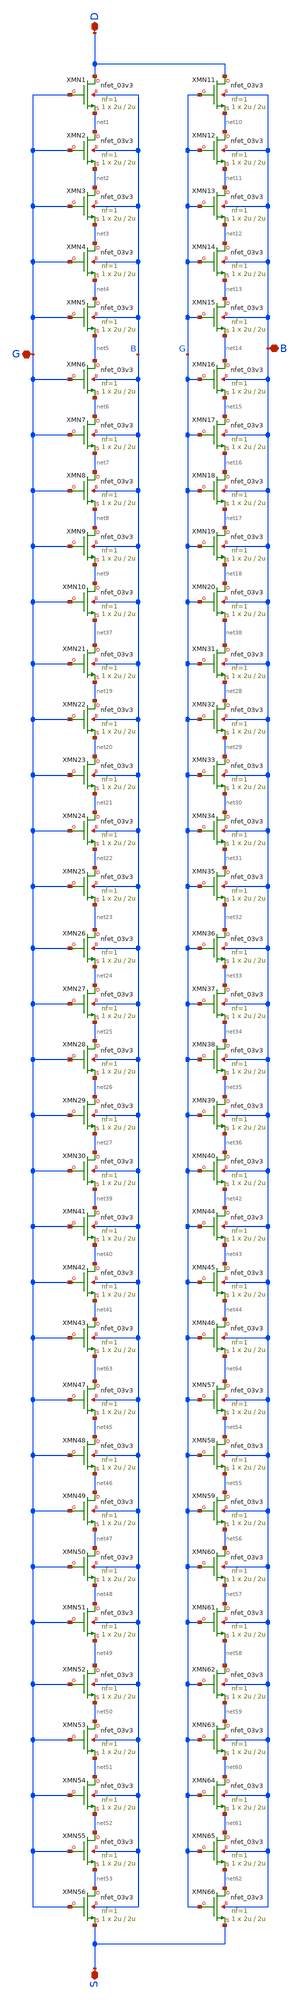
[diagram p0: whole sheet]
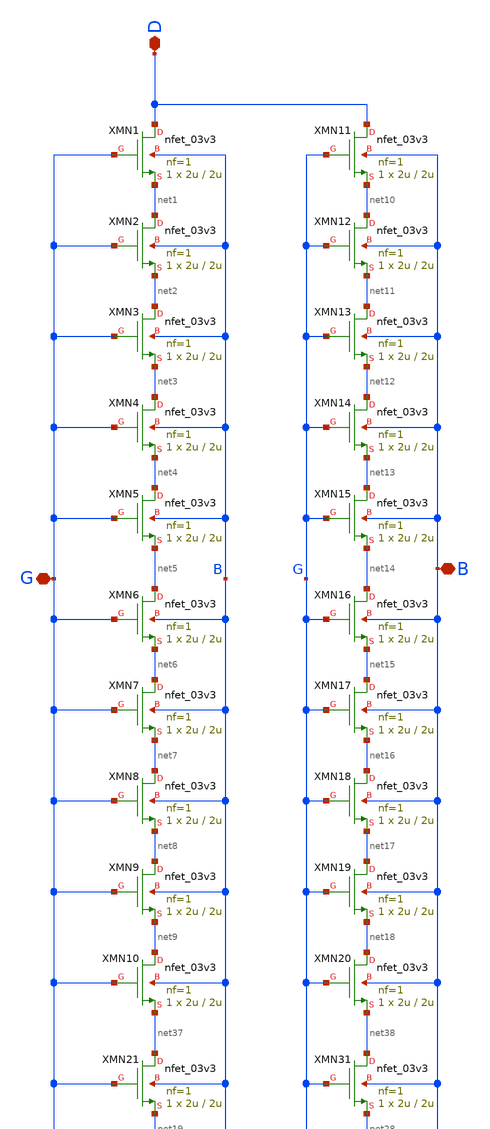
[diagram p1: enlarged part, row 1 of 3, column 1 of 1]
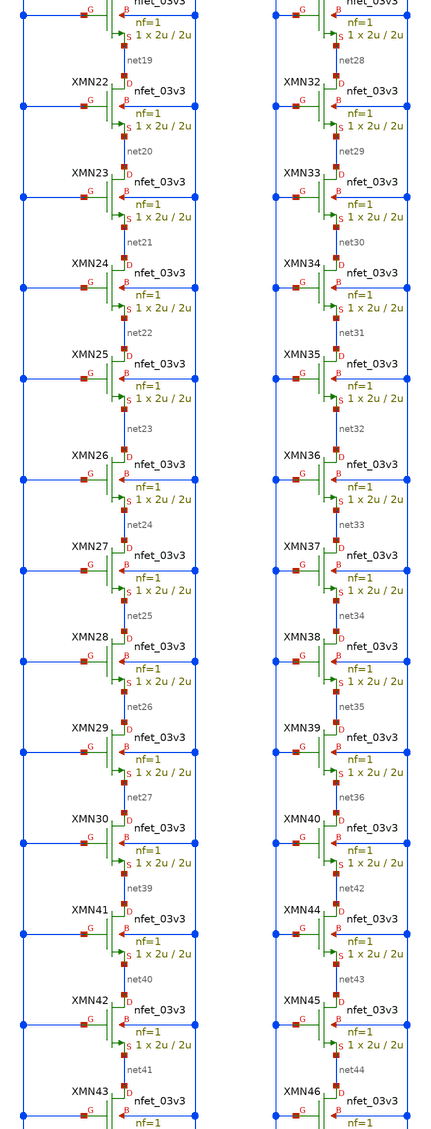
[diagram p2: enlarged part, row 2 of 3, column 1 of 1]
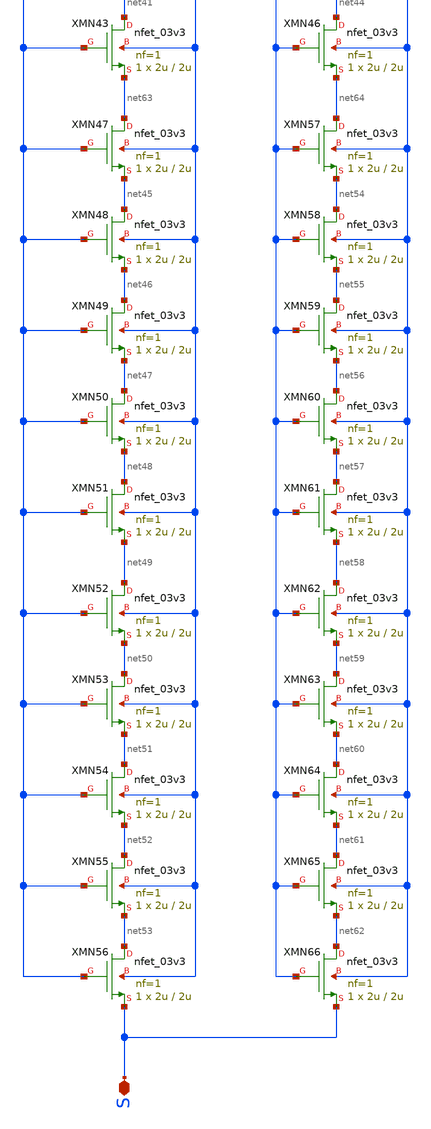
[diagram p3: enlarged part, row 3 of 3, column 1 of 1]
** sch_path: Voltage_Reference/symbols_vr/NMOS_matrix1_SCM1.sch
**.subckt NMOS_matrix1_SCM1 D G S B
*.iopin D
*.iopin G
*.iopin S
*.iopin B
XMN1 D G net1 B nfet_03v3 L=2u W=2u nf=1 ad='int((nf+1)/2) * W/nf * 0.18u' as='int((nf+2)/2) * W/nf * 0.18u'
+ pd='2*int((nf+1)/2) * (W/nf + 0.18u)' ps='2*int((nf+2)/2) * (W/nf + 0.18u)' nrd='0.18u / W' nrs='0.18u / W'
+ sa=0 sb=0 sd=0 m=1
XMN2 net1 G net2 B nfet_03v3 L=2u W=2u nf=1 ad='int((nf+1)/2) * W/nf * 0.18u' as='int((nf+2)/2) * W/nf * 0.18u'
+ pd='2*int((nf+1)/2) * (W/nf + 0.18u)' ps='2*int((nf+2)/2) * (W/nf + 0.18u)' nrd='0.18u / W' nrs='0.18u / W'
+ sa=0 sb=0 sd=0 m=1
XMN3 net2 G net3 B nfet_03v3 L=2u W=2u nf=1 ad='int((nf+1)/2) * W/nf * 0.18u' as='int((nf+2)/2) * W/nf * 0.18u'
+ pd='2*int((nf+1)/2) * (W/nf + 0.18u)' ps='2*int((nf+2)/2) * (W/nf + 0.18u)' nrd='0.18u / W' nrs='0.18u / W'
+ sa=0 sb=0 sd=0 m=1
XMN4 net3 G net4 B nfet_03v3 L=2u W=2u nf=1 ad='int((nf+1)/2) * W/nf * 0.18u' as='int((nf+2)/2) * W/nf * 0.18u'
+ pd='2*int((nf+1)/2) * (W/nf + 0.18u)' ps='2*int((nf+2)/2) * (W/nf + 0.18u)' nrd='0.18u / W' nrs='0.18u / W'
+ sa=0 sb=0 sd=0 m=1
XMN5 net4 G net5 B nfet_03v3 L=2u W=2u nf=1 ad='int((nf+1)/2) * W/nf * 0.18u' as='int((nf+2)/2) * W/nf * 0.18u'
+ pd='2*int((nf+1)/2) * (W/nf + 0.18u)' ps='2*int((nf+2)/2) * (W/nf + 0.18u)' nrd='0.18u / W' nrs='0.18u / W'
+ sa=0 sb=0 sd=0 m=1
XMN6 net5 G net6 B nfet_03v3 L=2u W=2u nf=1 ad='int((nf+1)/2) * W/nf * 0.18u' as='int((nf+2)/2) * W/nf * 0.18u'
+ pd='2*int((nf+1)/2) * (W/nf + 0.18u)' ps='2*int((nf+2)/2) * (W/nf + 0.18u)' nrd='0.18u / W' nrs='0.18u / W'
+ sa=0 sb=0 sd=0 m=1
XMN7 net6 G net7 B nfet_03v3 L=2u W=2u nf=1 ad='int((nf+1)/2) * W/nf * 0.18u' as='int((nf+2)/2) * W/nf * 0.18u'
+ pd='2*int((nf+1)/2) * (W/nf + 0.18u)' ps='2*int((nf+2)/2) * (W/nf + 0.18u)' nrd='0.18u / W' nrs='0.18u / W'
+ sa=0 sb=0 sd=0 m=1
XMN8 net7 G net8 B nfet_03v3 L=2u W=2u nf=1 ad='int((nf+1)/2) * W/nf * 0.18u' as='int((nf+2)/2) * W/nf * 0.18u'
+ pd='2*int((nf+1)/2) * (W/nf + 0.18u)' ps='2*int((nf+2)/2) * (W/nf + 0.18u)' nrd='0.18u / W' nrs='0.18u / W'
+ sa=0 sb=0 sd=0 m=1
XMN9 net8 G net9 B nfet_03v3 L=2u W=2u nf=1 ad='int((nf+1)/2) * W/nf * 0.18u' as='int((nf+2)/2) * W/nf * 0.18u'
+ pd='2*int((nf+1)/2) * (W/nf + 0.18u)' ps='2*int((nf+2)/2) * (W/nf + 0.18u)' nrd='0.18u / W' nrs='0.18u / W'
+ sa=0 sb=0 sd=0 m=1
XMN10 net9 G net37 B nfet_03v3 L=2u W=2u nf=1 ad='int((nf+1)/2) * W/nf * 0.18u' as='int((nf+2)/2) * W/nf * 0.18u'
+ pd='2*int((nf+1)/2) * (W/nf + 0.18u)' ps='2*int((nf+2)/2) * (W/nf + 0.18u)' nrd='0.18u / W' nrs='0.18u / W'
+ sa=0 sb=0 sd=0 m=1
XMN11 D G net10 B nfet_03v3 L=2u W=2u nf=1 ad='int((nf+1)/2) * W/nf * 0.18u' as='int((nf+2)/2) * W/nf * 0.18u'
+ pd='2*int((nf+1)/2) * (W/nf + 0.18u)' ps='2*int((nf+2)/2) * (W/nf + 0.18u)' nrd='0.18u / W' nrs='0.18u / W'
+ sa=0 sb=0 sd=0 m=1
XMN12 net10 G net11 B nfet_03v3 L=2u W=2u nf=1 ad='int((nf+1)/2) * W/nf * 0.18u' as='int((nf+2)/2) * W/nf * 0.18u'
+ pd='2*int((nf+1)/2) * (W/nf + 0.18u)' ps='2*int((nf+2)/2) * (W/nf + 0.18u)' nrd='0.18u / W' nrs='0.18u / W'
+ sa=0 sb=0 sd=0 m=1
XMN13 net11 G net12 B nfet_03v3 L=2u W=2u nf=1 ad='int((nf+1)/2) * W/nf * 0.18u' as='int((nf+2)/2) * W/nf * 0.18u'
+ pd='2*int((nf+1)/2) * (W/nf + 0.18u)' ps='2*int((nf+2)/2) * (W/nf + 0.18u)' nrd='0.18u / W' nrs='0.18u / W'
+ sa=0 sb=0 sd=0 m=1
XMN14 net12 G net13 B nfet_03v3 L=2u W=2u nf=1 ad='int((nf+1)/2) * W/nf * 0.18u' as='int((nf+2)/2) * W/nf * 0.18u'
+ pd='2*int((nf+1)/2) * (W/nf + 0.18u)' ps='2*int((nf+2)/2) * (W/nf + 0.18u)' nrd='0.18u / W' nrs='0.18u / W'
+ sa=0 sb=0 sd=0 m=1
XMN15 net13 G net14 B nfet_03v3 L=2u W=2u nf=1 ad='int((nf+1)/2) * W/nf * 0.18u' as='int((nf+2)/2) * W/nf * 0.18u'
+ pd='2*int((nf+1)/2) * (W/nf + 0.18u)' ps='2*int((nf+2)/2) * (W/nf + 0.18u)' nrd='0.18u / W' nrs='0.18u / W'
+ sa=0 sb=0 sd=0 m=1
XMN16 net14 G net15 B nfet_03v3 L=2u W=2u nf=1 ad='int((nf+1)/2) * W/nf * 0.18u' as='int((nf+2)/2) * W/nf * 0.18u'
+ pd='2*int((nf+1)/2) * (W/nf + 0.18u)' ps='2*int((nf+2)/2) * (W/nf + 0.18u)' nrd='0.18u / W' nrs='0.18u / W'
+ sa=0 sb=0 sd=0 m=1
XMN17 net15 G net16 B nfet_03v3 L=2u W=2u nf=1 ad='int((nf+1)/2) * W/nf * 0.18u' as='int((nf+2)/2) * W/nf * 0.18u'
+ pd='2*int((nf+1)/2) * (W/nf + 0.18u)' ps='2*int((nf+2)/2) * (W/nf + 0.18u)' nrd='0.18u / W' nrs='0.18u / W'
+ sa=0 sb=0 sd=0 m=1
XMN18 net16 G net17 B nfet_03v3 L=2u W=2u nf=1 ad='int((nf+1)/2) * W/nf * 0.18u' as='int((nf+2)/2) * W/nf * 0.18u'
+ pd='2*int((nf+1)/2) * (W/nf + 0.18u)' ps='2*int((nf+2)/2) * (W/nf + 0.18u)' nrd='0.18u / W' nrs='0.18u / W'
+ sa=0 sb=0 sd=0 m=1
XMN19 net17 G net18 B nfet_03v3 L=2u W=2u nf=1 ad='int((nf+1)/2) * W/nf * 0.18u' as='int((nf+2)/2) * W/nf * 0.18u'
+ pd='2*int((nf+1)/2) * (W/nf + 0.18u)' ps='2*int((nf+2)/2) * (W/nf + 0.18u)' nrd='0.18u / W' nrs='0.18u / W'
+ sa=0 sb=0 sd=0 m=1
XMN20 net18 G net38 B nfet_03v3 L=2u W=2u nf=1 ad='int((nf+1)/2) * W/nf * 0.18u' as='int((nf+2)/2) * W/nf * 0.18u'
+ pd='2*int((nf+1)/2) * (W/nf + 0.18u)' ps='2*int((nf+2)/2) * (W/nf + 0.18u)' nrd='0.18u / W' nrs='0.18u / W'
+ sa=0 sb=0 sd=0 m=1
XMN21 net37 G net19 B nfet_03v3 L=2u W=2u nf=1 ad='int((nf+1)/2) * W/nf * 0.18u' as='int((nf+2)/2) * W/nf * 0.18u'
+ pd='2*int((nf+1)/2) * (W/nf + 0.18u)' ps='2*int((nf+2)/2) * (W/nf + 0.18u)' nrd='0.18u / W' nrs='0.18u / W'
+ sa=0 sb=0 sd=0 m=1
XMN22 net19 G net20 B nfet_03v3 L=2u W=2u nf=1 ad='int((nf+1)/2) * W/nf * 0.18u' as='int((nf+2)/2) * W/nf * 0.18u'
+ pd='2*int((nf+1)/2) * (W/nf + 0.18u)' ps='2*int((nf+2)/2) * (W/nf + 0.18u)' nrd='0.18u / W' nrs='0.18u / W'
+ sa=0 sb=0 sd=0 m=1
XMN23 net20 G net21 B nfet_03v3 L=2u W=2u nf=1 ad='int((nf+1)/2) * W/nf * 0.18u' as='int((nf+2)/2) * W/nf * 0.18u'
+ pd='2*int((nf+1)/2) * (W/nf + 0.18u)' ps='2*int((nf+2)/2) * (W/nf + 0.18u)' nrd='0.18u / W' nrs='0.18u / W'
+ sa=0 sb=0 sd=0 m=1
XMN24 net21 G net22 B nfet_03v3 L=2u W=2u nf=1 ad='int((nf+1)/2) * W/nf * 0.18u' as='int((nf+2)/2) * W/nf * 0.18u'
+ pd='2*int((nf+1)/2) * (W/nf + 0.18u)' ps='2*int((nf+2)/2) * (W/nf + 0.18u)' nrd='0.18u / W' nrs='0.18u / W'
+ sa=0 sb=0 sd=0 m=1
XMN25 net22 G net23 B nfet_03v3 L=2u W=2u nf=1 ad='int((nf+1)/2) * W/nf * 0.18u' as='int((nf+2)/2) * W/nf * 0.18u'
+ pd='2*int((nf+1)/2) * (W/nf + 0.18u)' ps='2*int((nf+2)/2) * (W/nf + 0.18u)' nrd='0.18u / W' nrs='0.18u / W'
+ sa=0 sb=0 sd=0 m=1
XMN26 net23 G net24 B nfet_03v3 L=2u W=2u nf=1 ad='int((nf+1)/2) * W/nf * 0.18u' as='int((nf+2)/2) * W/nf * 0.18u'
+ pd='2*int((nf+1)/2) * (W/nf + 0.18u)' ps='2*int((nf+2)/2) * (W/nf + 0.18u)' nrd='0.18u / W' nrs='0.18u / W'
+ sa=0 sb=0 sd=0 m=1
XMN27 net24 G net25 B nfet_03v3 L=2u W=2u nf=1 ad='int((nf+1)/2) * W/nf * 0.18u' as='int((nf+2)/2) * W/nf * 0.18u'
+ pd='2*int((nf+1)/2) * (W/nf + 0.18u)' ps='2*int((nf+2)/2) * (W/nf + 0.18u)' nrd='0.18u / W' nrs='0.18u / W'
+ sa=0 sb=0 sd=0 m=1
XMN28 net25 G net26 B nfet_03v3 L=2u W=2u nf=1 ad='int((nf+1)/2) * W/nf * 0.18u' as='int((nf+2)/2) * W/nf * 0.18u'
+ pd='2*int((nf+1)/2) * (W/nf + 0.18u)' ps='2*int((nf+2)/2) * (W/nf + 0.18u)' nrd='0.18u / W' nrs='0.18u / W'
+ sa=0 sb=0 sd=0 m=1
XMN29 net26 G net27 B nfet_03v3 L=2u W=2u nf=1 ad='int((nf+1)/2) * W/nf * 0.18u' as='int((nf+2)/2) * W/nf * 0.18u'
+ pd='2*int((nf+1)/2) * (W/nf + 0.18u)' ps='2*int((nf+2)/2) * (W/nf + 0.18u)' nrd='0.18u / W' nrs='0.18u / W'
+ sa=0 sb=0 sd=0 m=1
XMN30 net27 G net39 B nfet_03v3 L=2u W=2u nf=1 ad='int((nf+1)/2) * W/nf * 0.18u' as='int((nf+2)/2) * W/nf * 0.18u'
+ pd='2*int((nf+1)/2) * (W/nf + 0.18u)' ps='2*int((nf+2)/2) * (W/nf + 0.18u)' nrd='0.18u / W' nrs='0.18u / W'
+ sa=0 sb=0 sd=0 m=1
XMN31 net38 G net28 B nfet_03v3 L=2u W=2u nf=1 ad='int((nf+1)/2) * W/nf * 0.18u' as='int((nf+2)/2) * W/nf * 0.18u'
+ pd='2*int((nf+1)/2) * (W/nf + 0.18u)' ps='2*int((nf+2)/2) * (W/nf + 0.18u)' nrd='0.18u / W' nrs='0.18u / W'
+ sa=0 sb=0 sd=0 m=1
XMN32 net28 G net29 B nfet_03v3 L=2u W=2u nf=1 ad='int((nf+1)/2) * W/nf * 0.18u' as='int((nf+2)/2) * W/nf * 0.18u'
+ pd='2*int((nf+1)/2) * (W/nf + 0.18u)' ps='2*int((nf+2)/2) * (W/nf + 0.18u)' nrd='0.18u / W' nrs='0.18u / W'
+ sa=0 sb=0 sd=0 m=1
XMN33 net29 G net30 B nfet_03v3 L=2u W=2u nf=1 ad='int((nf+1)/2) * W/nf * 0.18u' as='int((nf+2)/2) * W/nf * 0.18u'
+ pd='2*int((nf+1)/2) * (W/nf + 0.18u)' ps='2*int((nf+2)/2) * (W/nf + 0.18u)' nrd='0.18u / W' nrs='0.18u / W'
+ sa=0 sb=0 sd=0 m=1
XMN34 net30 G net31 B nfet_03v3 L=2u W=2u nf=1 ad='int((nf+1)/2) * W/nf * 0.18u' as='int((nf+2)/2) * W/nf * 0.18u'
+ pd='2*int((nf+1)/2) * (W/nf + 0.18u)' ps='2*int((nf+2)/2) * (W/nf + 0.18u)' nrd='0.18u / W' nrs='0.18u / W'
+ sa=0 sb=0 sd=0 m=1
XMN35 net31 G net32 B nfet_03v3 L=2u W=2u nf=1 ad='int((nf+1)/2) * W/nf * 0.18u' as='int((nf+2)/2) * W/nf * 0.18u'
+ pd='2*int((nf+1)/2) * (W/nf + 0.18u)' ps='2*int((nf+2)/2) * (W/nf + 0.18u)' nrd='0.18u / W' nrs='0.18u / W'
+ sa=0 sb=0 sd=0 m=1
XMN36 net32 G net33 B nfet_03v3 L=2u W=2u nf=1 ad='int((nf+1)/2) * W/nf * 0.18u' as='int((nf+2)/2) * W/nf * 0.18u'
+ pd='2*int((nf+1)/2) * (W/nf + 0.18u)' ps='2*int((nf+2)/2) * (W/nf + 0.18u)' nrd='0.18u / W' nrs='0.18u / W'
+ sa=0 sb=0 sd=0 m=1
XMN37 net33 G net34 B nfet_03v3 L=2u W=2u nf=1 ad='int((nf+1)/2) * W/nf * 0.18u' as='int((nf+2)/2) * W/nf * 0.18u'
+ pd='2*int((nf+1)/2) * (W/nf + 0.18u)' ps='2*int((nf+2)/2) * (W/nf + 0.18u)' nrd='0.18u / W' nrs='0.18u / W'
+ sa=0 sb=0 sd=0 m=1
XMN38 net34 G net35 B nfet_03v3 L=2u W=2u nf=1 ad='int((nf+1)/2) * W/nf * 0.18u' as='int((nf+2)/2) * W/nf * 0.18u'
+ pd='2*int((nf+1)/2) * (W/nf + 0.18u)' ps='2*int((nf+2)/2) * (W/nf + 0.18u)' nrd='0.18u / W' nrs='0.18u / W'
+ sa=0 sb=0 sd=0 m=1
XMN39 net35 G net36 B nfet_03v3 L=2u W=2u nf=1 ad='int((nf+1)/2) * W/nf * 0.18u' as='int((nf+2)/2) * W/nf * 0.18u'
+ pd='2*int((nf+1)/2) * (W/nf + 0.18u)' ps='2*int((nf+2)/2) * (W/nf + 0.18u)' nrd='0.18u / W' nrs='0.18u / W'
+ sa=0 sb=0 sd=0 m=1
XMN40 net36 G net42 B nfet_03v3 L=2u W=2u nf=1 ad='int((nf+1)/2) * W/nf * 0.18u' as='int((nf+2)/2) * W/nf * 0.18u'
+ pd='2*int((nf+1)/2) * (W/nf + 0.18u)' ps='2*int((nf+2)/2) * (W/nf + 0.18u)' nrd='0.18u / W' nrs='0.18u / W'
+ sa=0 sb=0 sd=0 m=1
XMN41 net39 G net40 B nfet_03v3 L=2u W=2u nf=1 ad='int((nf+1)/2) * W/nf * 0.18u' as='int((nf+2)/2) * W/nf * 0.18u'
+ pd='2*int((nf+1)/2) * (W/nf + 0.18u)' ps='2*int((nf+2)/2) * (W/nf + 0.18u)' nrd='0.18u / W' nrs='0.18u / W'
+ sa=0 sb=0 sd=0 m=1
XMN42 net40 G net41 B nfet_03v3 L=2u W=2u nf=1 ad='int((nf+1)/2) * W/nf * 0.18u' as='int((nf+2)/2) * W/nf * 0.18u'
+ pd='2*int((nf+1)/2) * (W/nf + 0.18u)' ps='2*int((nf+2)/2) * (W/nf + 0.18u)' nrd='0.18u / W' nrs='0.18u / W'
+ sa=0 sb=0 sd=0 m=1
XMN43 net41 G net63 B nfet_03v3 L=2u W=2u nf=1 ad='int((nf+1)/2) * W/nf * 0.18u' as='int((nf+2)/2) * W/nf * 0.18u'
+ pd='2*int((nf+1)/2) * (W/nf + 0.18u)' ps='2*int((nf+2)/2) * (W/nf + 0.18u)' nrd='0.18u / W' nrs='0.18u / W'
+ sa=0 sb=0 sd=0 m=1
XMN44 net42 G net43 B nfet_03v3 L=2u W=2u nf=1 ad='int((nf+1)/2) * W/nf * 0.18u' as='int((nf+2)/2) * W/nf * 0.18u'
+ pd='2*int((nf+1)/2) * (W/nf + 0.18u)' ps='2*int((nf+2)/2) * (W/nf + 0.18u)' nrd='0.18u / W' nrs='0.18u / W'
+ sa=0 sb=0 sd=0 m=1
XMN45 net43 G net44 B nfet_03v3 L=2u W=2u nf=1 ad='int((nf+1)/2) * W/nf * 0.18u' as='int((nf+2)/2) * W/nf * 0.18u'
+ pd='2*int((nf+1)/2) * (W/nf + 0.18u)' ps='2*int((nf+2)/2) * (W/nf + 0.18u)' nrd='0.18u / W' nrs='0.18u / W'
+ sa=0 sb=0 sd=0 m=1
XMN46 net44 G net64 B nfet_03v3 L=2u W=2u nf=1 ad='int((nf+1)/2) * W/nf * 0.18u' as='int((nf+2)/2) * W/nf * 0.18u'
+ pd='2*int((nf+1)/2) * (W/nf + 0.18u)' ps='2*int((nf+2)/2) * (W/nf + 0.18u)' nrd='0.18u / W' nrs='0.18u / W'
+ sa=0 sb=0 sd=0 m=1
XMN47 net63 G net45 B nfet_03v3 L=2u W=2u nf=1 ad='int((nf+1)/2) * W/nf * 0.18u' as='int((nf+2)/2) * W/nf * 0.18u'
+ pd='2*int((nf+1)/2) * (W/nf + 0.18u)' ps='2*int((nf+2)/2) * (W/nf + 0.18u)' nrd='0.18u / W' nrs='0.18u / W'
+ sa=0 sb=0 sd=0 m=1
XMN48 net45 G net46 B nfet_03v3 L=2u W=2u nf=1 ad='int((nf+1)/2) * W/nf * 0.18u' as='int((nf+2)/2) * W/nf * 0.18u'
+ pd='2*int((nf+1)/2) * (W/nf + 0.18u)' ps='2*int((nf+2)/2) * (W/nf + 0.18u)' nrd='0.18u / W' nrs='0.18u / W'
+ sa=0 sb=0 sd=0 m=1
XMN49 net46 G net47 B nfet_03v3 L=2u W=2u nf=1 ad='int((nf+1)/2) * W/nf * 0.18u' as='int((nf+2)/2) * W/nf * 0.18u'
+ pd='2*int((nf+1)/2) * (W/nf + 0.18u)' ps='2*int((nf+2)/2) * (W/nf + 0.18u)' nrd='0.18u / W' nrs='0.18u / W'
+ sa=0 sb=0 sd=0 m=1
XMN50 net47 G net48 B nfet_03v3 L=2u W=2u nf=1 ad='int((nf+1)/2) * W/nf * 0.18u' as='int((nf+2)/2) * W/nf * 0.18u'
+ pd='2*int((nf+1)/2) * (W/nf + 0.18u)' ps='2*int((nf+2)/2) * (W/nf + 0.18u)' nrd='0.18u / W' nrs='0.18u / W'
+ sa=0 sb=0 sd=0 m=1
XMN51 net48 G net49 B nfet_03v3 L=2u W=2u nf=1 ad='int((nf+1)/2) * W/nf * 0.18u' as='int((nf+2)/2) * W/nf * 0.18u'
+ pd='2*int((nf+1)/2) * (W/nf + 0.18u)' ps='2*int((nf+2)/2) * (W/nf + 0.18u)' nrd='0.18u / W' nrs='0.18u / W'
+ sa=0 sb=0 sd=0 m=1
XMN52 net49 G net50 B nfet_03v3 L=2u W=2u nf=1 ad='int((nf+1)/2) * W/nf * 0.18u' as='int((nf+2)/2) * W/nf * 0.18u'
+ pd='2*int((nf+1)/2) * (W/nf + 0.18u)' ps='2*int((nf+2)/2) * (W/nf + 0.18u)' nrd='0.18u / W' nrs='0.18u / W'
+ sa=0 sb=0 sd=0 m=1
XMN53 net50 G net51 B nfet_03v3 L=2u W=2u nf=1 ad='int((nf+1)/2) * W/nf * 0.18u' as='int((nf+2)/2) * W/nf * 0.18u'
+ pd='2*int((nf+1)/2) * (W/nf + 0.18u)' ps='2*int((nf+2)/2) * (W/nf + 0.18u)' nrd='0.18u / W' nrs='0.18u / W'
+ sa=0 sb=0 sd=0 m=1
XMN54 net51 G net52 B nfet_03v3 L=2u W=2u nf=1 ad='int((nf+1)/2) * W/nf * 0.18u' as='int((nf+2)/2) * W/nf * 0.18u'
+ pd='2*int((nf+1)/2) * (W/nf + 0.18u)' ps='2*int((nf+2)/2) * (W/nf + 0.18u)' nrd='0.18u / W' nrs='0.18u / W'
+ sa=0 sb=0 sd=0 m=1
XMN55 net52 G net53 B nfet_03v3 L=2u W=2u nf=1 ad='int((nf+1)/2) * W/nf * 0.18u' as='int((nf+2)/2) * W/nf * 0.18u'
+ pd='2*int((nf+1)/2) * (W/nf + 0.18u)' ps='2*int((nf+2)/2) * (W/nf + 0.18u)' nrd='0.18u / W' nrs='0.18u / W'
+ sa=0 sb=0 sd=0 m=1
XMN56 net53 G S B nfet_03v3 L=2u W=2u nf=1 ad='int((nf+1)/2) * W/nf * 0.18u' as='int((nf+2)/2) * W/nf * 0.18u'
+ pd='2*int((nf+1)/2) * (W/nf + 0.18u)' ps='2*int((nf+2)/2) * (W/nf + 0.18u)' nrd='0.18u / W' nrs='0.18u / W'
+ sa=0 sb=0 sd=0 m=1
XMN57 net64 G net54 B nfet_03v3 L=2u W=2u nf=1 ad='int((nf+1)/2) * W/nf * 0.18u' as='int((nf+2)/2) * W/nf * 0.18u'
+ pd='2*int((nf+1)/2) * (W/nf + 0.18u)' ps='2*int((nf+2)/2) * (W/nf + 0.18u)' nrd='0.18u / W' nrs='0.18u / W'
+ sa=0 sb=0 sd=0 m=1
XMN58 net54 G net55 B nfet_03v3 L=2u W=2u nf=1 ad='int((nf+1)/2) * W/nf * 0.18u' as='int((nf+2)/2) * W/nf * 0.18u'
+ pd='2*int((nf+1)/2) * (W/nf + 0.18u)' ps='2*int((nf+2)/2) * (W/nf + 0.18u)' nrd='0.18u / W' nrs='0.18u / W'
+ sa=0 sb=0 sd=0 m=1
XMN59 net55 G net56 B nfet_03v3 L=2u W=2u nf=1 ad='int((nf+1)/2) * W/nf * 0.18u' as='int((nf+2)/2) * W/nf * 0.18u'
+ pd='2*int((nf+1)/2) * (W/nf + 0.18u)' ps='2*int((nf+2)/2) * (W/nf + 0.18u)' nrd='0.18u / W' nrs='0.18u / W'
+ sa=0 sb=0 sd=0 m=1
XMN60 net56 G net57 B nfet_03v3 L=2u W=2u nf=1 ad='int((nf+1)/2) * W/nf * 0.18u' as='int((nf+2)/2) * W/nf * 0.18u'
+ pd='2*int((nf+1)/2) * (W/nf + 0.18u)' ps='2*int((nf+2)/2) * (W/nf + 0.18u)' nrd='0.18u / W' nrs='0.18u / W'
+ sa=0 sb=0 sd=0 m=1
XMN61 net57 G net58 B nfet_03v3 L=2u W=2u nf=1 ad='int((nf+1)/2) * W/nf * 0.18u' as='int((nf+2)/2) * W/nf * 0.18u'
+ pd='2*int((nf+1)/2) * (W/nf + 0.18u)' ps='2*int((nf+2)/2) * (W/nf + 0.18u)' nrd='0.18u / W' nrs='0.18u / W'
+ sa=0 sb=0 sd=0 m=1
XMN62 net58 G net59 B nfet_03v3 L=2u W=2u nf=1 ad='int((nf+1)/2) * W/nf * 0.18u' as='int((nf+2)/2) * W/nf * 0.18u'
+ pd='2*int((nf+1)/2) * (W/nf + 0.18u)' ps='2*int((nf+2)/2) * (W/nf + 0.18u)' nrd='0.18u / W' nrs='0.18u / W'
+ sa=0 sb=0 sd=0 m=1
XMN63 net59 G net60 B nfet_03v3 L=2u W=2u nf=1 ad='int((nf+1)/2) * W/nf * 0.18u' as='int((nf+2)/2) * W/nf * 0.18u'
+ pd='2*int((nf+1)/2) * (W/nf + 0.18u)' ps='2*int((nf+2)/2) * (W/nf + 0.18u)' nrd='0.18u / W' nrs='0.18u / W'
+ sa=0 sb=0 sd=0 m=1
XMN64 net60 G net61 B nfet_03v3 L=2u W=2u nf=1 ad='int((nf+1)/2) * W/nf * 0.18u' as='int((nf+2)/2) * W/nf * 0.18u'
+ pd='2*int((nf+1)/2) * (W/nf + 0.18u)' ps='2*int((nf+2)/2) * (W/nf + 0.18u)' nrd='0.18u / W' nrs='0.18u / W'
+ sa=0 sb=0 sd=0 m=1
XMN65 net61 G net62 B nfet_03v3 L=2u W=2u nf=1 ad='int((nf+1)/2) * W/nf * 0.18u' as='int((nf+2)/2) * W/nf * 0.18u'
+ pd='2*int((nf+1)/2) * (W/nf + 0.18u)' ps='2*int((nf+2)/2) * (W/nf + 0.18u)' nrd='0.18u / W' nrs='0.18u / W'
+ sa=0 sb=0 sd=0 m=1
XMN66 net62 G S B nfet_03v3 L=2u W=2u nf=1 ad='int((nf+1)/2) * W/nf * 0.18u' as='int((nf+2)/2) * W/nf * 0.18u'
+ pd='2*int((nf+1)/2) * (W/nf + 0.18u)' ps='2*int((nf+2)/2) * (W/nf + 0.18u)' nrd='0.18u / W' nrs='0.18u / W'
+ sa=0 sb=0 sd=0 m=1
**.ends
.end
